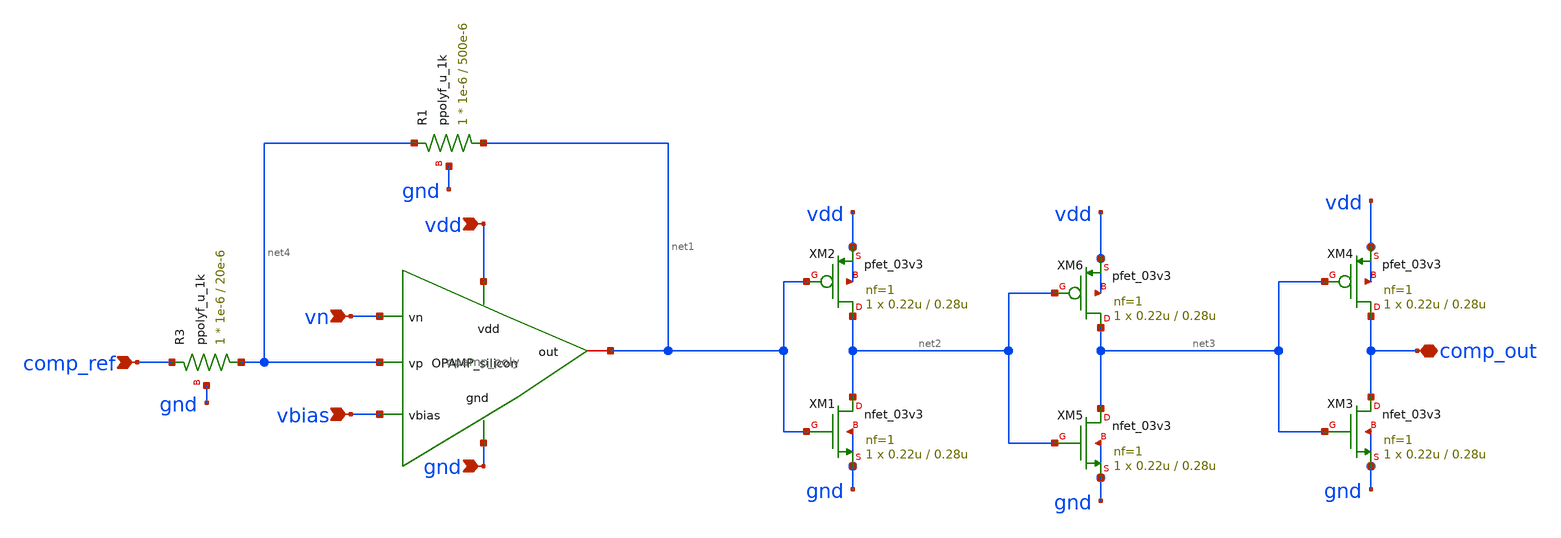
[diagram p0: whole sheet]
** sch_path: xschem/comparator/comp.sch
**.subckt comp vn vbias vdd comp_ref comp_out gnd
*.ipin vn
*.ipin vbias
*.ipin vdd
*.ipin comp_ref
*.iopin comp_out
*.ipin gnd
XM1 net2 net1 gnd gnd nfet_03v3 L=0.28u W=0.22u nf=1 ad='int((nf+1)/2) * W/nf * 0.18u' as='int((nf+2)/2) * W/nf * 0.18u'
+ pd='2*int((nf+1)/2) * (W/nf + 0.18u)' ps='2*int((nf+2)/2) * (W/nf + 0.18u)' nrd='0.18u / W' nrs='0.18u / W'
+ sa=0 sb=0 sd=0 m=1
XM2 net2 net1 vdd vdd pfet_03v3 L=0.28u W=0.22u nf=1 ad='int((nf+1)/2) * W/nf * 0.18u' as='int((nf+2)/2) * W/nf * 0.18u'
+ pd='2*int((nf+1)/2) * (W/nf + 0.18u)' ps='2*int((nf+2)/2) * (W/nf + 0.18u)' nrd='0.18u / W' nrs='0.18u / W'
+ sa=0 sb=0 sd=0 m=1
XM5 net3 net2 gnd gnd nfet_03v3 L=0.28u W=0.22u nf=1 ad='int((nf+1)/2) * W/nf * 0.18u' as='int((nf+2)/2) * W/nf * 0.18u'
+ pd='2*int((nf+1)/2) * (W/nf + 0.18u)' ps='2*int((nf+2)/2) * (W/nf + 0.18u)' nrd='0.18u / W' nrs='0.18u / W'
+ sa=0 sb=0 sd=0 m=1
XM6 net3 net2 vdd vdd pfet_03v3 L=0.28u W=0.22u nf=1 ad='int((nf+1)/2) * W/nf * 0.18u' as='int((nf+2)/2) * W/nf * 0.18u'
+ pd='2*int((nf+1)/2) * (W/nf + 0.18u)' ps='2*int((nf+2)/2) * (W/nf + 0.18u)' nrd='0.18u / W' nrs='0.18u / W'
+ sa=0 sb=0 sd=0 m=1
x1 vdd vn gnd net1 net4 vbias opamp_poly
XR3 net4 comp_ref gnd ppolyf_u_1k r_width=1e-6 r_length=20e-6 m=1
XR1 net1 net4 gnd ppolyf_u_1k r_width=1e-6 r_length=500e-6 m=1
XM3 comp_out net3 gnd gnd nfet_03v3 L=0.28u W=0.22u nf=1 ad='int((nf+1)/2) * W/nf * 0.18u' as='int((nf+2)/2) * W/nf * 0.18u'
+ pd='2*int((nf+1)/2) * (W/nf + 0.18u)' ps='2*int((nf+2)/2) * (W/nf + 0.18u)' nrd='0.18u / W' nrs='0.18u / W'
+ sa=0 sb=0 sd=0 m=1
XM4 comp_out net3 vdd vdd pfet_03v3 L=0.28u W=0.22u nf=1 ad='int((nf+1)/2) * W/nf * 0.18u' as='int((nf+2)/2) * W/nf * 0.18u'
+ pd='2*int((nf+1)/2) * (W/nf + 0.18u)' ps='2*int((nf+2)/2) * (W/nf + 0.18u)' nrd='0.18u / W' nrs='0.18u / W'
+ sa=0 sb=0 sd=0 m=1
**.ends

* expanding   symbol:  GF180/xschem/Chipathon/OpAMP_Silicon/opamp_poly.sym # of pins=6
** sym_path: OpAmP/opamp_poly.sym
** sch_path: OpAmP/opamp_poly.sch
.subckt opamp_poly vdd vn gnd out vp vbias
*.ipin gnd
*.iopin out
*.ipin vbias
*.ipin vp
*.ipin vn
*.ipin vdd
XM1 net3 vbias gnd gnd nfet_03v3 L=l1 W=w1 nf=1 ad='int((nf+1)/2) * W/nf * 0.18u' as='int((nf+2)/2) * W/nf * 0.18u'
+ pd='2*int((nf+1)/2) * (W/nf + 0.18u)' ps='2*int((nf+2)/2) * (W/nf + 0.18u)' nrd='0.18u / W' nrs='0.18u / W'
+ sa=0 sb=0 sd=0 m=1
XM2 net2 net2 vdd vdd pfet_03v3 L=l2 W=w2 nf=1 ad='int((nf+1)/2) * W/nf * 0.18u' as='int((nf+2)/2) * W/nf * 0.18u'
+ pd='2*int((nf+1)/2) * (W/nf + 0.18u)' ps='2*int((nf+2)/2) * (W/nf + 0.18u)' nrd='0.18u / W' nrs='0.18u / W'
+ sa=0 sb=0 sd=0 m=1
XM3 out vbias gnd gnd nfet_03v3 L=l3 W=w3 nf=1 ad='int((nf+1)/2) * W/nf * 0.18u' as='int((nf+2)/2) * W/nf * 0.18u'
+ pd='2*int((nf+1)/2) * (W/nf + 0.18u)' ps='2*int((nf+2)/2) * (W/nf + 0.18u)' nrd='0.18u / W' nrs='0.18u / W'
+ sa=0 sb=0 sd=0 m=1
XM4 net2 vn net3 gnd nfet_03v3 L=l4 W=w4 nf=1 ad='int((nf+1)/2) * W/nf * 0.18u' as='int((nf+2)/2) * W/nf * 0.18u'
+ pd='2*int((nf+1)/2) * (W/nf + 0.18u)' ps='2*int((nf+2)/2) * (W/nf + 0.18u)' nrd='0.18u / W' nrs='0.18u / W'
+ sa=0 sb=0 sd=0 m=1
XM5 net1 vp net3 gnd nfet_03v3 L=l5 W=w5 nf=1 ad='int((nf+1)/2) * W/nf * 0.18u' as='int((nf+2)/2) * W/nf * 0.18u'
+ pd='2*int((nf+1)/2) * (W/nf + 0.18u)' ps='2*int((nf+2)/2) * (W/nf + 0.18u)' nrd='0.18u / W' nrs='0.18u / W'
+ sa=0 sb=0 sd=0 m=1
XM6 net1 net2 vdd vdd pfet_03v3 L=l6 W=w6 nf=1 ad='int((nf+1)/2) * W/nf * 0.18u' as='int((nf+2)/2) * W/nf * 0.18u'
+ pd='2*int((nf+1)/2) * (W/nf + 0.18u)' ps='2*int((nf+2)/2) * (W/nf + 0.18u)' nrd='0.18u / W' nrs='0.18u / W'
+ sa=0 sb=0 sd=0 m=1
XM7 out net1 vdd vdd pfet_03v3 L=l7 W=w7 nf=1 ad='int((nf+1)/2) * W/nf * 0.18u' as='int((nf+2)/2) * W/nf * 0.18u'
+ pd='2*int((nf+1)/2) * (W/nf + 0.18u)' ps='2*int((nf+2)/2) * (W/nf + 0.18u)' nrd='0.18u / W' nrs='0.18u / W'
+ sa=0 sb=0 sd=0 m=1
XR1 net4 net1 gnd ppolyf_u_1k r_width=3e-6 r_length=6.6e-6 m=1
XC1 out net4 cap_mim_1f5fF c_width=20e-6 c_length=20e-6 m=1
.ends

.end
